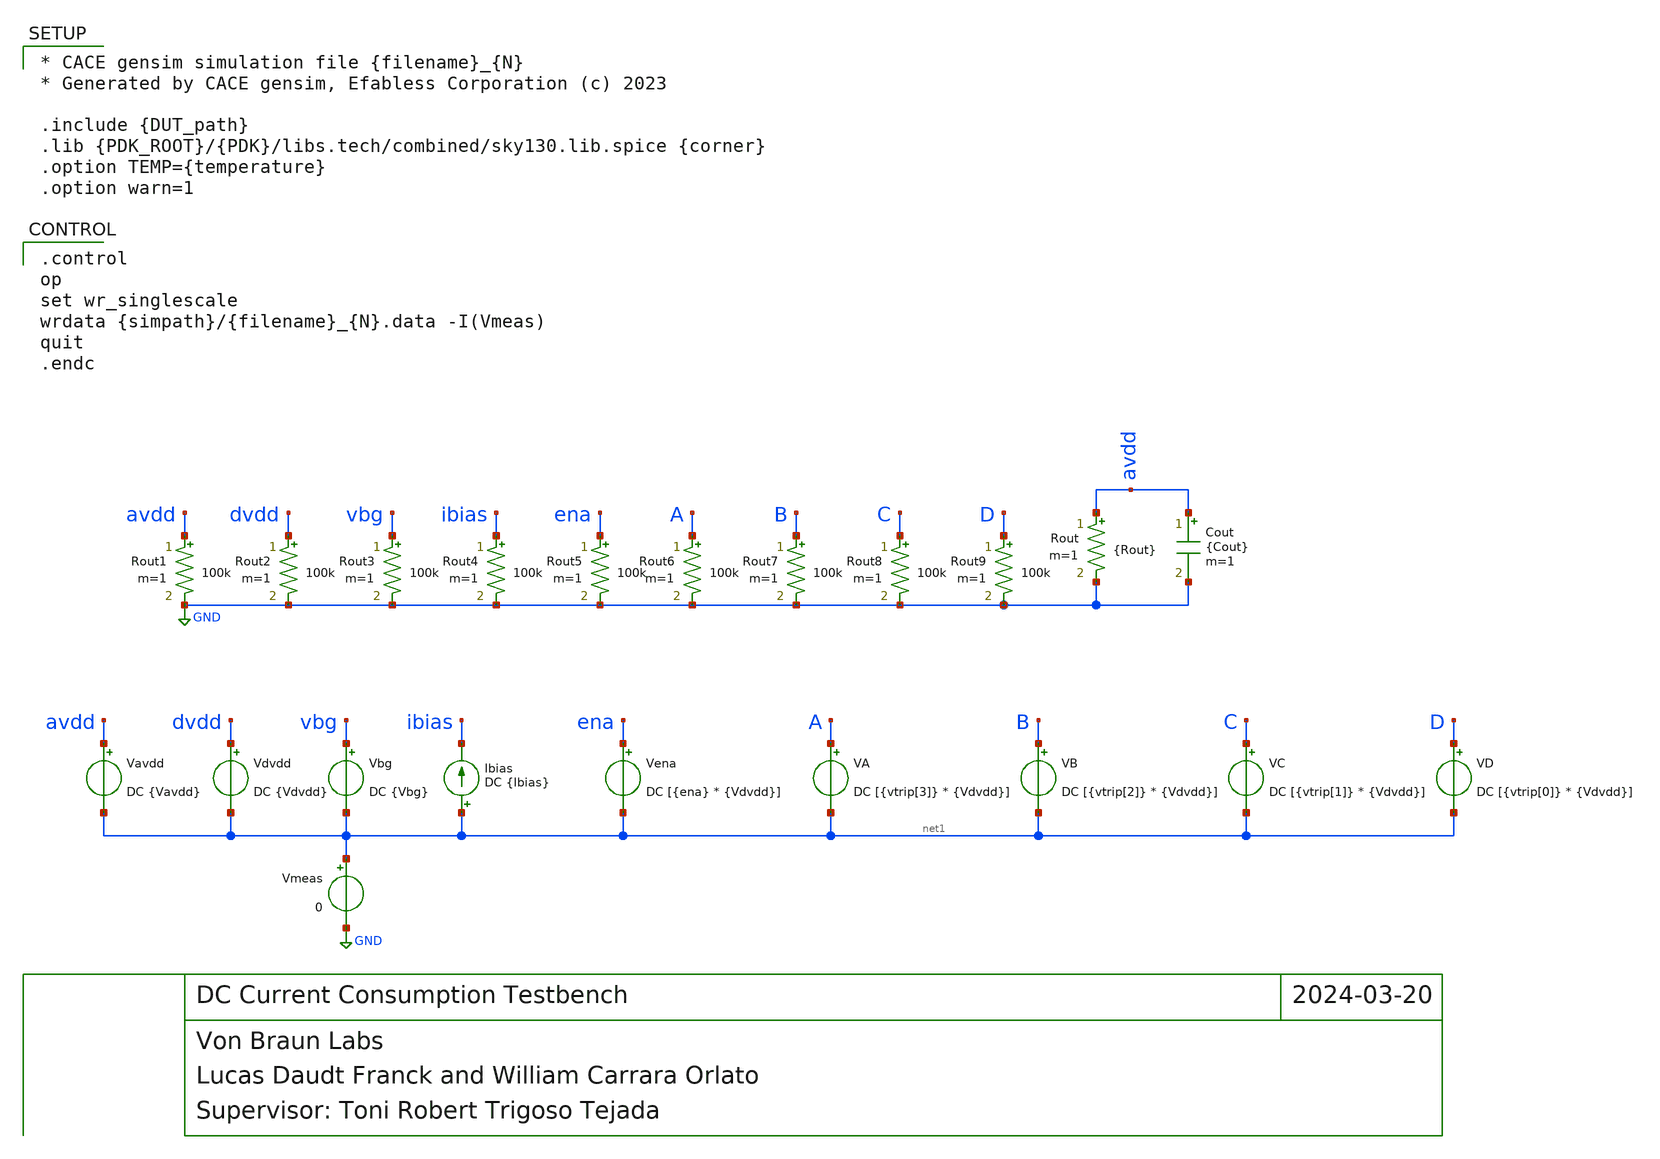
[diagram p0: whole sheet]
** sch_path: cace/tb_dccurrent.sch
**.subckt tb_dccurrent
Cout avdd GND {Cout} m=1
Rout avdd GND {Rout} m=1
Vavdd avdd net1 DC {Vavdd}
Vdvdd dvdd net1 DC {Vdvdd}
Vena ena net1 DC [{ena} * {Vdvdd}]
VA A net1 DC [{vtrip[3]} * {Vdvdd}]
VB B net1 DC [{vtrip[2]} * {Vdvdd}]
VC C net1 DC [{vtrip[1]} * {Vdvdd}]
VD D net1 DC [{vtrip[0]} * {Vdvdd}]
Vbg vbg net1 DC {Vbg}
Ibias net1 ibias DC {Ibias}
Rout1 avdd GND 100k m=1
Rout2 dvdd GND 100k m=1
Rout3 vbg GND 100k m=1
Rout4 ibias GND 100k m=1
Rout5 ena GND 100k m=1
Rout6 A GND 100k m=1
Rout7 B GND 100k m=1
Rout8 C GND 100k m=1
Rout9 D GND 100k m=1
Vmeas net1 GND 0
**** begin user architecture code

* CACE gensim simulation file {filename}_{N}
* Generated by CACE gensim, Efabless Corporation (c) 2023

.include {DUT_path}
.lib {PDK_ROOT}/{PDK}/libs.tech/combined/sky130.lib.spice {corner}
.option TEMP={temperature}
.option warn=1



.control
op
set wr_singlescale
wrdata {simpath}/{filename}_{N}.data -I(Vmeas)
quit
.endc


**** end user architecture code
**.ends
.GLOBAL GND
.end
